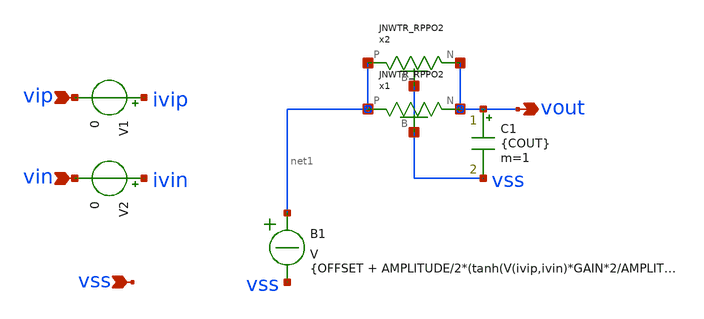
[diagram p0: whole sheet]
** sch_path: sim/TB_Vref/OTAideal.sch
**.subckt OTAideal vip vin vss vout
*.ipin vip
*.ipin vin
*.ipin vss
*.opin vout
B1 net1 vss V = {OFFSET + AMPLITUDE/2*(tanh(V(ivip,ivin)*GAIN*2/AMPLITUDE))}
V1 ivip vip 0
V2 ivin vin 0
C1 vout vss {COUT} m=1
x1 vout net1 vss JNWTR_RPPO2
x2 vout net1 vss JNWTR_RPPO2
**.ends
.end
